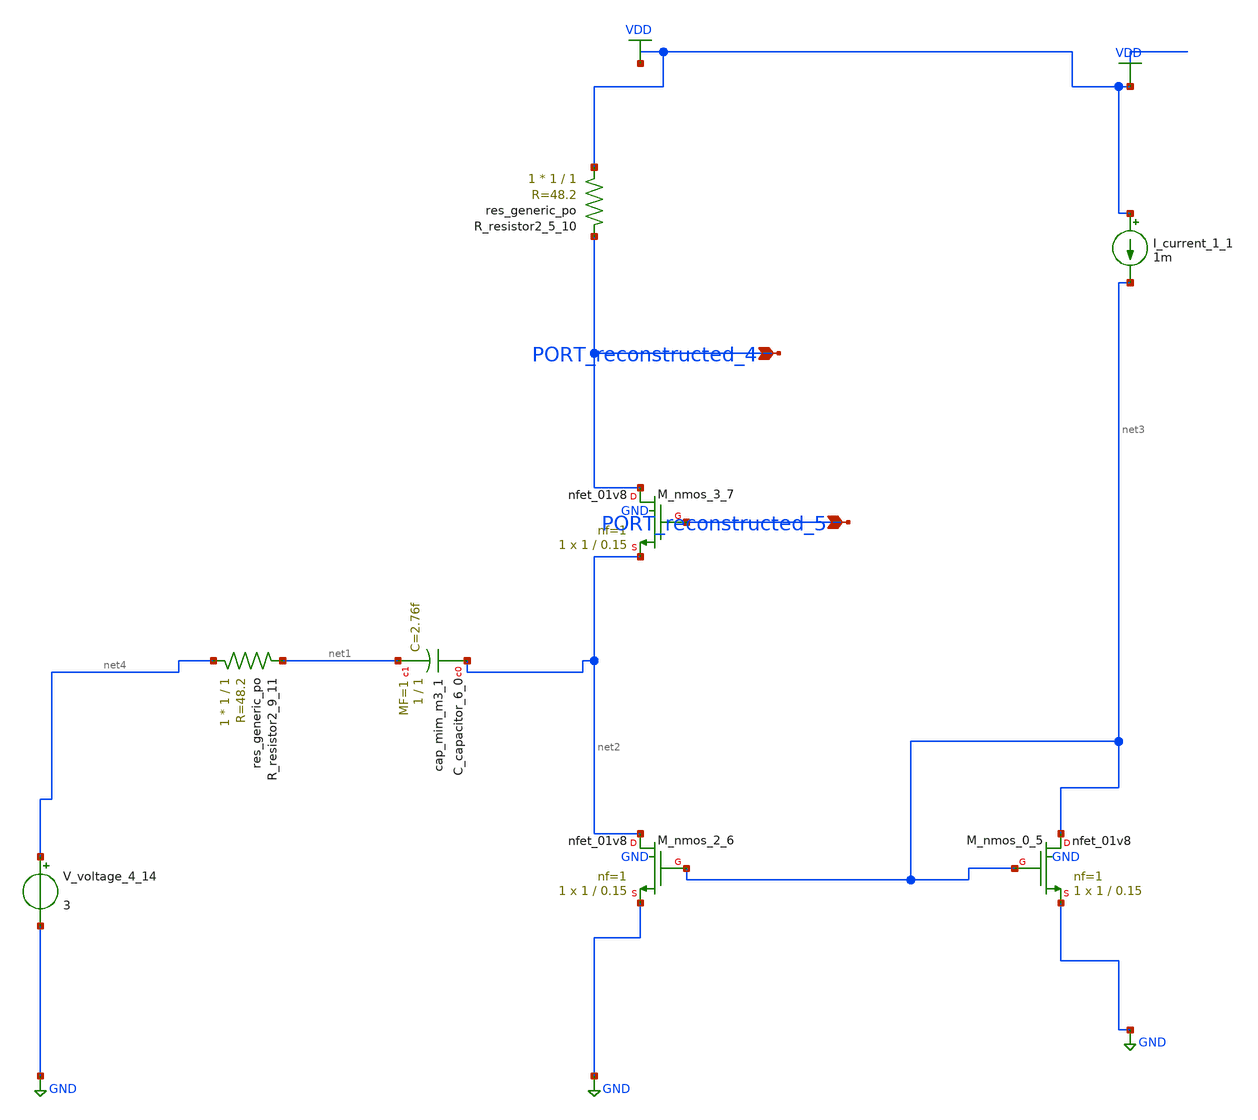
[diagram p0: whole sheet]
** sch_path: schematics/AMSNet/313.sch
**.subckt 313 PORT_reconstructed_5 PORT_reconstructed_4
*.ipin PORT_reconstructed_5
*.ipin PORT_reconstructed_4
XC_capacitor_6_0 net2 net1 sky130_fd_pr__cap_mim_m3_1 W=1 L=1 MF=1 m=1
I_current_1_1 VDD net3 1m
XM_nmos_0_5 net3 net3 GND GND sky130_fd_pr__nfet_01v8 L=0.15 W=1 nf=1 ad='int((1 + 1)/2) * 1 / 1 * 0.29'
+ as='int((1 + 2)/2) * 1 / 1 * 0.29' pd='2*int((1 + 1)/2) * (1 / 1 + 0.29)' ps='2*int((1 + 2)/2) * (1 / 1 + 0.29)'
+ nrd='0.29 / 1 ' nrs='0.29 / 1 ' sa=0 sb=0 sd=0 mult=1 m=1
XM_nmos_2_6 net2 net3 GND GND sky130_fd_pr__nfet_01v8 L=0.15 W=1 nf=1 ad='int((1 + 1)/2) * 1 / 1 * 0.29'
+ as='int((1 + 2)/2) * 1 / 1 * 0.29' pd='2*int((1 + 1)/2) * (1 / 1 + 0.29)' ps='2*int((1 + 2)/2) * (1 / 1 + 0.29)'
+ nrd='0.29 / 1 ' nrs='0.29 / 1 ' sa=0 sb=0 sd=0 mult=1 m=1
XM_nmos_3_7 PORT_reconstructed_4 PORT_reconstructed_5 net2 GND sky130_fd_pr__nfet_01v8 L=0.15 W=1 nf=1
+ ad='int((1 + 1)/2) * 1 / 1 * 0.29' as='int((1 + 2)/2) * 1 / 1 * 0.29' pd='2*int((1 + 1)/2) * (1 / 1 + 0.29)'
+ ps='2*int((1 + 2)/2) * (1 / 1 + 0.29)' nrd='0.29 / 1 ' nrs='0.29 / 1 ' sa=0 sb=0 sd=0 mult=1 m=1
XR_resistor2_5_10 VDD PORT_reconstructed_4 sky130_fd_pr__res_generic_po W=1 L=1 m=1
XR_resistor2_9_11 net4 net1 sky130_fd_pr__res_generic_po W=1 L=1 m=1
V_voltage_4_14 net4 GND 3
**.ends
.GLOBAL GND
.GLOBAL VDD
.end
